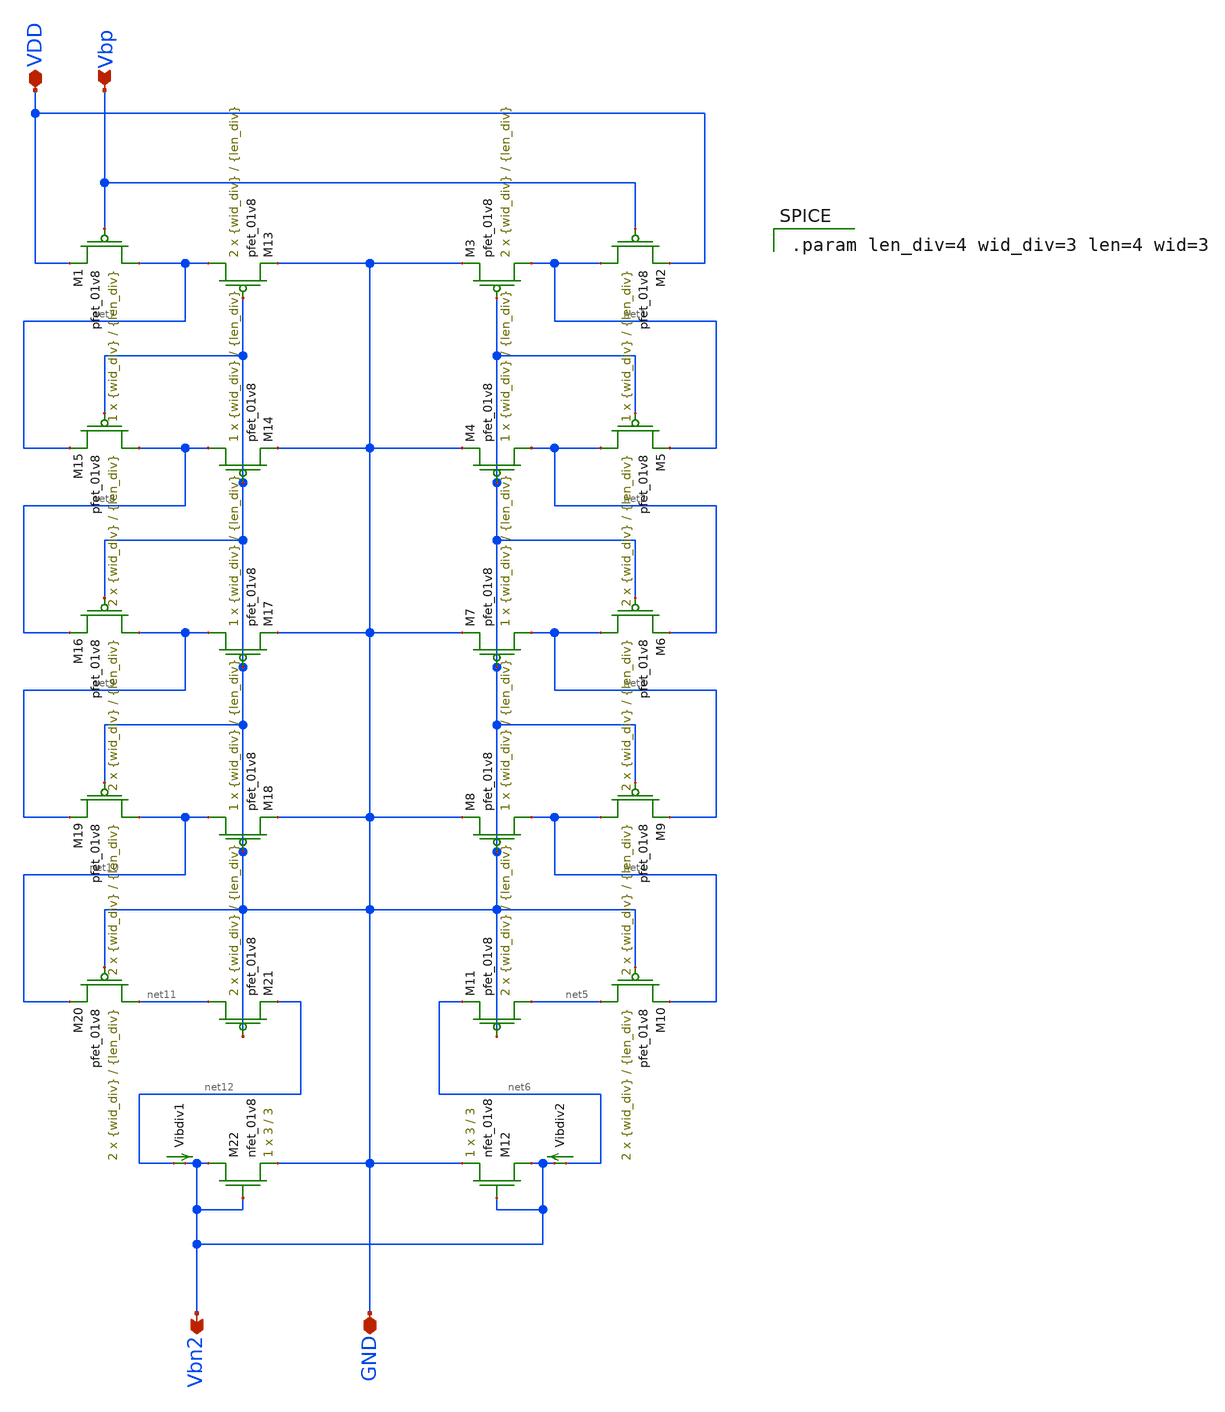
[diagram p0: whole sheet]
** sch_path: mp3/Layout_Schem_Designs/current_divider_lds.sch
**.subckt current_divider_lds GND Vbn2 Vbp VDD
*.iopin GND
*.opin Vbn2
*.ipin Vbp
*.iopin VDD
XM2 net1 Vbp VDD VDD sky130_fd_pr__pfet_01v8 L={len_div} W={wid_div} nf=1 ad='int((nf+1)/2) * W/nf * 0.29'
+ as='int((nf+2)/2) * W/nf * 0.29' pd='2*int((nf+1)/2) * (W/nf + 0.29)' ps='2*int((nf+2)/2) * (W/nf + 0.29)'
+ nrd='0.29 / W' nrs='0.29 / W' sa=0 sb=0 sd=0 mult=1 m=1
XM3 net1 GND GND VDD sky130_fd_pr__pfet_01v8 L={len_div} W={wid_div} nf=1 ad='int((nf+1)/2) * W/nf * 0.29'
+ as='int((nf+2)/2) * W/nf * 0.29' pd='2*int((nf+1)/2) * (W/nf + 0.29)' ps='2*int((nf+2)/2) * (W/nf + 0.29)'
+ nrd='0.29 / W' nrs='0.29 / W' sa=0 sb=0 sd=0 mult=2 m=2
XM4 net2 GND GND VDD sky130_fd_pr__pfet_01v8 L={len_div} W={wid_div} nf=1 ad='int((nf+1)/2) * W/nf * 0.29'
+ as='int((nf+2)/2) * W/nf * 0.29' pd='2*int((nf+1)/2) * (W/nf + 0.29)' ps='2*int((nf+2)/2) * (W/nf + 0.29)'
+ nrd='0.29 / W' nrs='0.29 / W' sa=0 sb=0 sd=0 mult=1 m=1
XM5 net2 GND net1 VDD sky130_fd_pr__pfet_01v8 L={len_div} W={wid_div} nf=1 ad='int((nf+1)/2) * W/nf * 0.29'
+ as='int((nf+2)/2) * W/nf * 0.29' pd='2*int((nf+1)/2) * (W/nf + 0.29)' ps='2*int((nf+2)/2) * (W/nf + 0.29)'
+ nrd='0.29 / W' nrs='0.29 / W' sa=0 sb=0 sd=0 mult=2 m=2
XM6 net3 GND net2 VDD sky130_fd_pr__pfet_01v8 L={len_div} W={wid_div} nf=1 ad='int((nf+1)/2) * W/nf * 0.29'
+ as='int((nf+2)/2) * W/nf * 0.29' pd='2*int((nf+1)/2) * (W/nf + 0.29)' ps='2*int((nf+2)/2) * (W/nf + 0.29)'
+ nrd='0.29 / W' nrs='0.29 / W' sa=0 sb=0 sd=0 mult=2 m=2
XM7 net3 GND GND VDD sky130_fd_pr__pfet_01v8 L={len_div} W={wid_div} nf=1 ad='int((nf+1)/2) * W/nf * 0.29'
+ as='int((nf+2)/2) * W/nf * 0.29' pd='2*int((nf+1)/2) * (W/nf + 0.29)' ps='2*int((nf+2)/2) * (W/nf + 0.29)'
+ nrd='0.29 / W' nrs='0.29 / W' sa=0 sb=0 sd=0 mult=1 m=1
XM8 net4 GND GND VDD sky130_fd_pr__pfet_01v8 L={len_div} W={wid_div} nf=1 ad='int((nf+1)/2) * W/nf * 0.29'
+ as='int((nf+2)/2) * W/nf * 0.29' pd='2*int((nf+1)/2) * (W/nf + 0.29)' ps='2*int((nf+2)/2) * (W/nf + 0.29)'
+ nrd='0.29 / W' nrs='0.29 / W' sa=0 sb=0 sd=0 mult=1 m=1
XM9 net4 GND net3 VDD sky130_fd_pr__pfet_01v8 L={len_div} W={wid_div} nf=1 ad='int((nf+1)/2) * W/nf * 0.29'
+ as='int((nf+2)/2) * W/nf * 0.29' pd='2*int((nf+1)/2) * (W/nf + 0.29)' ps='2*int((nf+2)/2) * (W/nf + 0.29)'
+ nrd='0.29 / W' nrs='0.29 / W' sa=0 sb=0 sd=0 mult=2 m=2
XM10 net5 GND net4 VDD sky130_fd_pr__pfet_01v8 L={len_div} W={wid_div} nf=1 ad='int((nf+1)/2) * W/nf * 0.29'
+ as='int((nf+2)/2) * W/nf * 0.29' pd='2*int((nf+1)/2) * (W/nf + 0.29)' ps='2*int((nf+2)/2) * (W/nf + 0.29)'
+ nrd='0.29 / W' nrs='0.29 / W' sa=0 sb=0 sd=0 mult=2 m=2
XM11 net5 GND net6 VDD sky130_fd_pr__pfet_01v8 L={len_div} W={wid_div} nf=1 ad='int((nf+1)/2) * W/nf * 0.29'
+ as='int((nf+2)/2) * W/nf * 0.29' pd='2*int((nf+1)/2) * (W/nf + 0.29)' ps='2*int((nf+2)/2) * (W/nf + 0.29)'
+ nrd='0.29 / W' nrs='0.29 / W' sa=0 sb=0 sd=0 mult=2 m=2
XM12 Vbn2 Vbn2 GND GND sky130_fd_pr__nfet_01v8 L=3 W=3 nf=1 ad='int((nf+1)/2) * W/nf * 0.29' as='int((nf+2)/2) * W/nf * 0.29'
+ pd='2*int((nf+1)/2) * (W/nf + 0.29)' ps='2*int((nf+2)/2) * (W/nf + 0.29)' nrd='0.29 / W' nrs='0.29 / W'
+ sa=0 sb=0 sd=0 mult=1 m=1
Vibdiv2 net6 Vbn2 0
.save i(vibdiv2)
XM1 net7 Vbp VDD VDD sky130_fd_pr__pfet_01v8 L={len_div} W={wid_div} nf=1 ad='int((nf+1)/2) * W/nf * 0.29'
+ as='int((nf+2)/2) * W/nf * 0.29' pd='2*int((nf+1)/2) * (W/nf + 0.29)' ps='2*int((nf+2)/2) * (W/nf + 0.29)'
+ nrd='0.29 / W' nrs='0.29 / W' sa=0 sb=0 sd=0 mult=1 m=1
XM13 net7 GND GND VDD sky130_fd_pr__pfet_01v8 L={len_div} W={wid_div} nf=1 ad='int((nf+1)/2) * W/nf * 0.29'
+ as='int((nf+2)/2) * W/nf * 0.29' pd='2*int((nf+1)/2) * (W/nf + 0.29)' ps='2*int((nf+2)/2) * (W/nf + 0.29)'
+ nrd='0.29 / W' nrs='0.29 / W' sa=0 sb=0 sd=0 mult=2 m=2
XM14 net8 GND GND VDD sky130_fd_pr__pfet_01v8 L={len_div} W={wid_div} nf=1 ad='int((nf+1)/2) * W/nf * 0.29'
+ as='int((nf+2)/2) * W/nf * 0.29' pd='2*int((nf+1)/2) * (W/nf + 0.29)' ps='2*int((nf+2)/2) * (W/nf + 0.29)'
+ nrd='0.29 / W' nrs='0.29 / W' sa=0 sb=0 sd=0 mult=1 m=1
XM15 net8 GND net7 VDD sky130_fd_pr__pfet_01v8 L={len_div} W={wid_div} nf=1 ad='int((nf+1)/2) * W/nf * 0.29'
+ as='int((nf+2)/2) * W/nf * 0.29' pd='2*int((nf+1)/2) * (W/nf + 0.29)' ps='2*int((nf+2)/2) * (W/nf + 0.29)'
+ nrd='0.29 / W' nrs='0.29 / W' sa=0 sb=0 sd=0 mult=2 m=2
XM16 net9 GND net8 VDD sky130_fd_pr__pfet_01v8 L={len_div} W={wid_div} nf=1 ad='int((nf+1)/2) * W/nf * 0.29'
+ as='int((nf+2)/2) * W/nf * 0.29' pd='2*int((nf+1)/2) * (W/nf + 0.29)' ps='2*int((nf+2)/2) * (W/nf + 0.29)'
+ nrd='0.29 / W' nrs='0.29 / W' sa=0 sb=0 sd=0 mult=2 m=2
XM17 net9 GND GND VDD sky130_fd_pr__pfet_01v8 L={len_div} W={wid_div} nf=1 ad='int((nf+1)/2) * W/nf * 0.29'
+ as='int((nf+2)/2) * W/nf * 0.29' pd='2*int((nf+1)/2) * (W/nf + 0.29)' ps='2*int((nf+2)/2) * (W/nf + 0.29)'
+ nrd='0.29 / W' nrs='0.29 / W' sa=0 sb=0 sd=0 mult=1 m=1
XM18 net10 GND GND VDD sky130_fd_pr__pfet_01v8 L={len_div} W={wid_div} nf=1 ad='int((nf+1)/2) * W/nf * 0.29'
+ as='int((nf+2)/2) * W/nf * 0.29' pd='2*int((nf+1)/2) * (W/nf + 0.29)' ps='2*int((nf+2)/2) * (W/nf + 0.29)'
+ nrd='0.29 / W' nrs='0.29 / W' sa=0 sb=0 sd=0 mult=1 m=1
XM19 net10 GND net9 VDD sky130_fd_pr__pfet_01v8 L={len_div} W={wid_div} nf=1 ad='int((nf+1)/2) * W/nf * 0.29'
+ as='int((nf+2)/2) * W/nf * 0.29' pd='2*int((nf+1)/2) * (W/nf + 0.29)' ps='2*int((nf+2)/2) * (W/nf + 0.29)'
+ nrd='0.29 / W' nrs='0.29 / W' sa=0 sb=0 sd=0 mult=2 m=2
XM20 net11 GND net10 VDD sky130_fd_pr__pfet_01v8 L={len_div} W={wid_div} nf=1 ad='int((nf+1)/2) * W/nf * 0.29'
+ as='int((nf+2)/2) * W/nf * 0.29' pd='2*int((nf+1)/2) * (W/nf + 0.29)' ps='2*int((nf+2)/2) * (W/nf + 0.29)'
+ nrd='0.29 / W' nrs='0.29 / W' sa=0 sb=0 sd=0 mult=2 m=2
XM21 net11 GND net12 VDD sky130_fd_pr__pfet_01v8 L={len_div} W={wid_div} nf=1 ad='int((nf+1)/2) * W/nf * 0.29'
+ as='int((nf+2)/2) * W/nf * 0.29' pd='2*int((nf+1)/2) * (W/nf + 0.29)' ps='2*int((nf+2)/2) * (W/nf + 0.29)'
+ nrd='0.29 / W' nrs='0.29 / W' sa=0 sb=0 sd=0 mult=2 m=2
XM22 Vbn2 Vbn2 GND GND sky130_fd_pr__nfet_01v8 L=3 W=3 nf=1 ad='int((nf+1)/2) * W/nf * 0.29' as='int((nf+2)/2) * W/nf * 0.29'
+ pd='2*int((nf+1)/2) * (W/nf + 0.29)' ps='2*int((nf+2)/2) * (W/nf + 0.29)' nrd='0.29 / W' nrs='0.29 / W'
+ sa=0 sb=0 sd=0 mult=1 m=1
Vibdiv1 net12 Vbn2 0
.save i(vibdiv1)
**** begin user architecture code

.param len_div=4 wid_div=3 len=4 wid=3

**** end user architecture code
**.ends
.end
